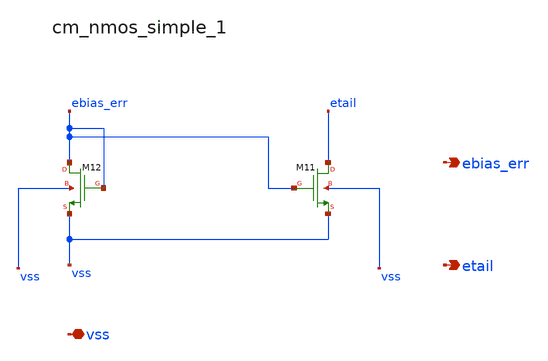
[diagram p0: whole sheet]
** sch_path: analog-db/raw/ldo_005_buffered_ref/hier/blocks/cm_nmos_simple_1.sch
**.subckt cm_nmos_simple_1 vss ebias_err etail
*.iopin vss
*.opin ebias_err
*.opin etail
XM11 etail ebias_err vss vss sg13_lv_nmos w=x_dut_xm11_w l=x_dut_xm11_l ng=1 m=1
XM12 ebias_err ebias_err vss vss sg13_lv_nmos w=x_dut_xm12_w l=x_dut_xm12_l ng=1 m=1
**.ends
.end
